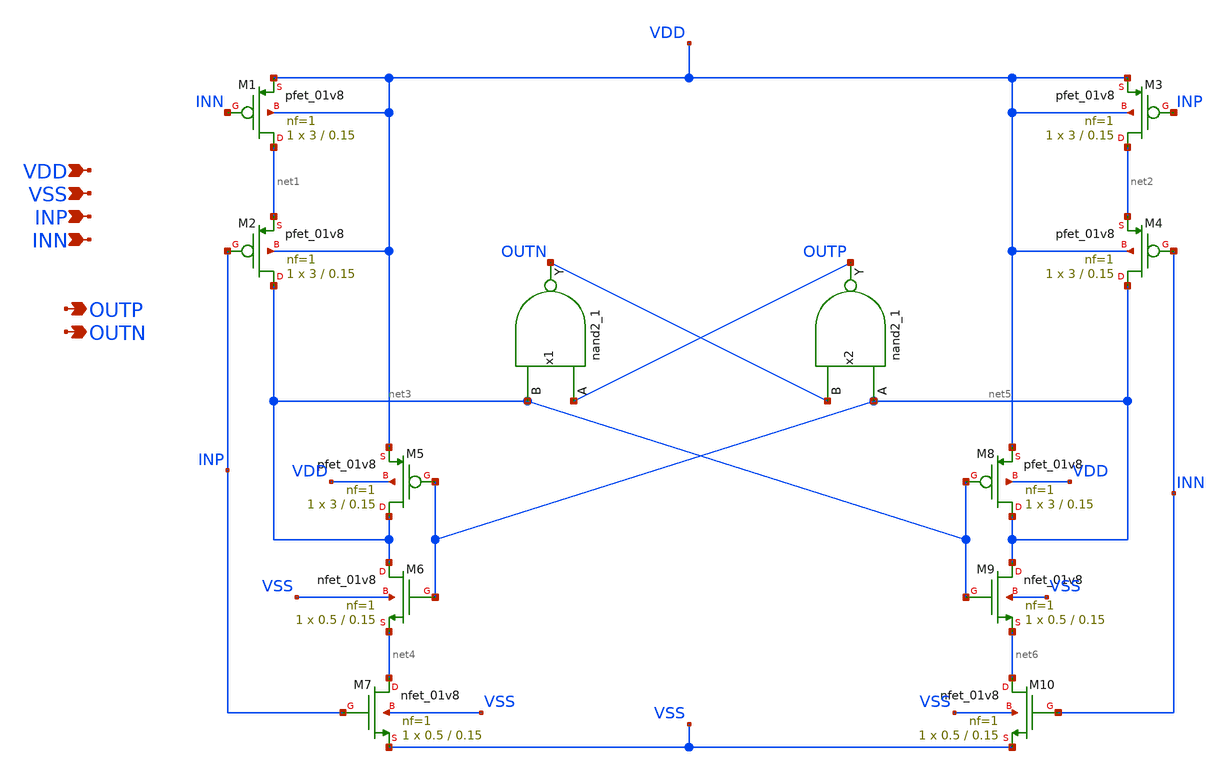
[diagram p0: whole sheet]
** sch_path: xschem/phase_detector.sch
**.subckt phase_detector VDD INP INN VSS OUTP OUTN
*.ipin VDD
*.ipin INP
*.ipin INN
*.ipin VSS
*.opin OUTP
*.opin OUTN
XM7 net4 INP VSS VSS sky130_fd_pr__nfet_01v8 L=0.15 W=0.5 nf=1 ad='int((nf+1)/2) * W/nf * 0.29' as='int((nf+2)/2) * W/nf * 0.29'
+ pd='2*int((nf+1)/2) * (W/nf + 0.29)' ps='2*int((nf+2)/2) * (W/nf + 0.29)' nrd='0.29 / W' nrs='0.29 / W'
+ sa=0 sb=0 sd=0 mult=1 m=1
XM6 net3 net5 net4 VSS sky130_fd_pr__nfet_01v8 L=0.15 W=0.5 nf=1 ad='int((nf+1)/2) * W/nf * 0.29' as='int((nf+2)/2) * W/nf * 0.29'
+ pd='2*int((nf+1)/2) * (W/nf + 0.29)' ps='2*int((nf+2)/2) * (W/nf + 0.29)' nrd='0.29 / W' nrs='0.29 / W'
+ sa=0 sb=0 sd=0 mult=1 m=1
XM9 net5 net3 net6 VSS sky130_fd_pr__nfet_01v8 L=0.15 W=0.5 nf=1 ad='int((nf+1)/2) * W/nf * 0.29' as='int((nf+2)/2) * W/nf * 0.29'
+ pd='2*int((nf+1)/2) * (W/nf + 0.29)' ps='2*int((nf+2)/2) * (W/nf + 0.29)' nrd='0.29 / W' nrs='0.29 / W'
+ sa=0 sb=0 sd=0 mult=1 m=1
XM10 net6 INN VSS VSS sky130_fd_pr__nfet_01v8 L=0.15 W=0.5 nf=1 ad='int((nf+1)/2) * W/nf * 0.29' as='int((nf+2)/2) * W/nf * 0.29'
+ pd='2*int((nf+1)/2) * (W/nf + 0.29)' ps='2*int((nf+2)/2) * (W/nf + 0.29)' nrd='0.29 / W' nrs='0.29 / W'
+ sa=0 sb=0 sd=0 mult=1 m=1
XM1 net1 INN VDD VDD sky130_fd_pr__pfet_01v8 L=0.15 W=3 nf=1 ad='int((nf+1)/2) * W/nf * 0.29' as='int((nf+2)/2) * W/nf * 0.29'
+ pd='2*int((nf+1)/2) * (W/nf + 0.29)' ps='2*int((nf+2)/2) * (W/nf + 0.29)' nrd='0.29 / W' nrs='0.29 / W'
+ sa=0 sb=0 sd=0 mult=1 m=1
XM2 net3 INP net1 VDD sky130_fd_pr__pfet_01v8 L=0.15 W=3 nf=1 ad='int((nf+1)/2) * W/nf * 0.29' as='int((nf+2)/2) * W/nf * 0.29'
+ pd='2*int((nf+1)/2) * (W/nf + 0.29)' ps='2*int((nf+2)/2) * (W/nf + 0.29)' nrd='0.29 / W' nrs='0.29 / W'
+ sa=0 sb=0 sd=0 mult=1 m=1
XM3 net2 INP VDD VDD sky130_fd_pr__pfet_01v8 L=0.15 W=3 nf=1 ad='int((nf+1)/2) * W/nf * 0.29' as='int((nf+2)/2) * W/nf * 0.29'
+ pd='2*int((nf+1)/2) * (W/nf + 0.29)' ps='2*int((nf+2)/2) * (W/nf + 0.29)' nrd='0.29 / W' nrs='0.29 / W'
+ sa=0 sb=0 sd=0 mult=1 m=1
XM4 net5 INN net2 VDD sky130_fd_pr__pfet_01v8 L=0.15 W=3 nf=1 ad='int((nf+1)/2) * W/nf * 0.29' as='int((nf+2)/2) * W/nf * 0.29'
+ pd='2*int((nf+1)/2) * (W/nf + 0.29)' ps='2*int((nf+2)/2) * (W/nf + 0.29)' nrd='0.29 / W' nrs='0.29 / W'
+ sa=0 sb=0 sd=0 mult=1 m=1
XM5 net3 net5 VDD VDD sky130_fd_pr__pfet_01v8 L=0.15 W=3 nf=1 ad='int((nf+1)/2) * W/nf * 0.29' as='int((nf+2)/2) * W/nf * 0.29'
+ pd='2*int((nf+1)/2) * (W/nf + 0.29)' ps='2*int((nf+2)/2) * (W/nf + 0.29)' nrd='0.29 / W' nrs='0.29 / W'
+ sa=0 sb=0 sd=0 mult=1 m=1
XM8 net5 net3 VDD VDD sky130_fd_pr__pfet_01v8 L=0.15 W=3 nf=1 ad='int((nf+1)/2) * W/nf * 0.29' as='int((nf+2)/2) * W/nf * 0.29'
+ pd='2*int((nf+1)/2) * (W/nf + 0.29)' ps='2*int((nf+2)/2) * (W/nf + 0.29)' nrd='0.29 / W' nrs='0.29 / W'
+ sa=0 sb=0 sd=0 mult=1 m=1
x1 OUTP net3 VSS VSS VDD VDD OUTN sky130_fd_sc_hd__nand2_1
x2 net5 OUTN VSS VSS VDD VDD OUTP sky130_fd_sc_hd__nand2_1
**.ends
.end
